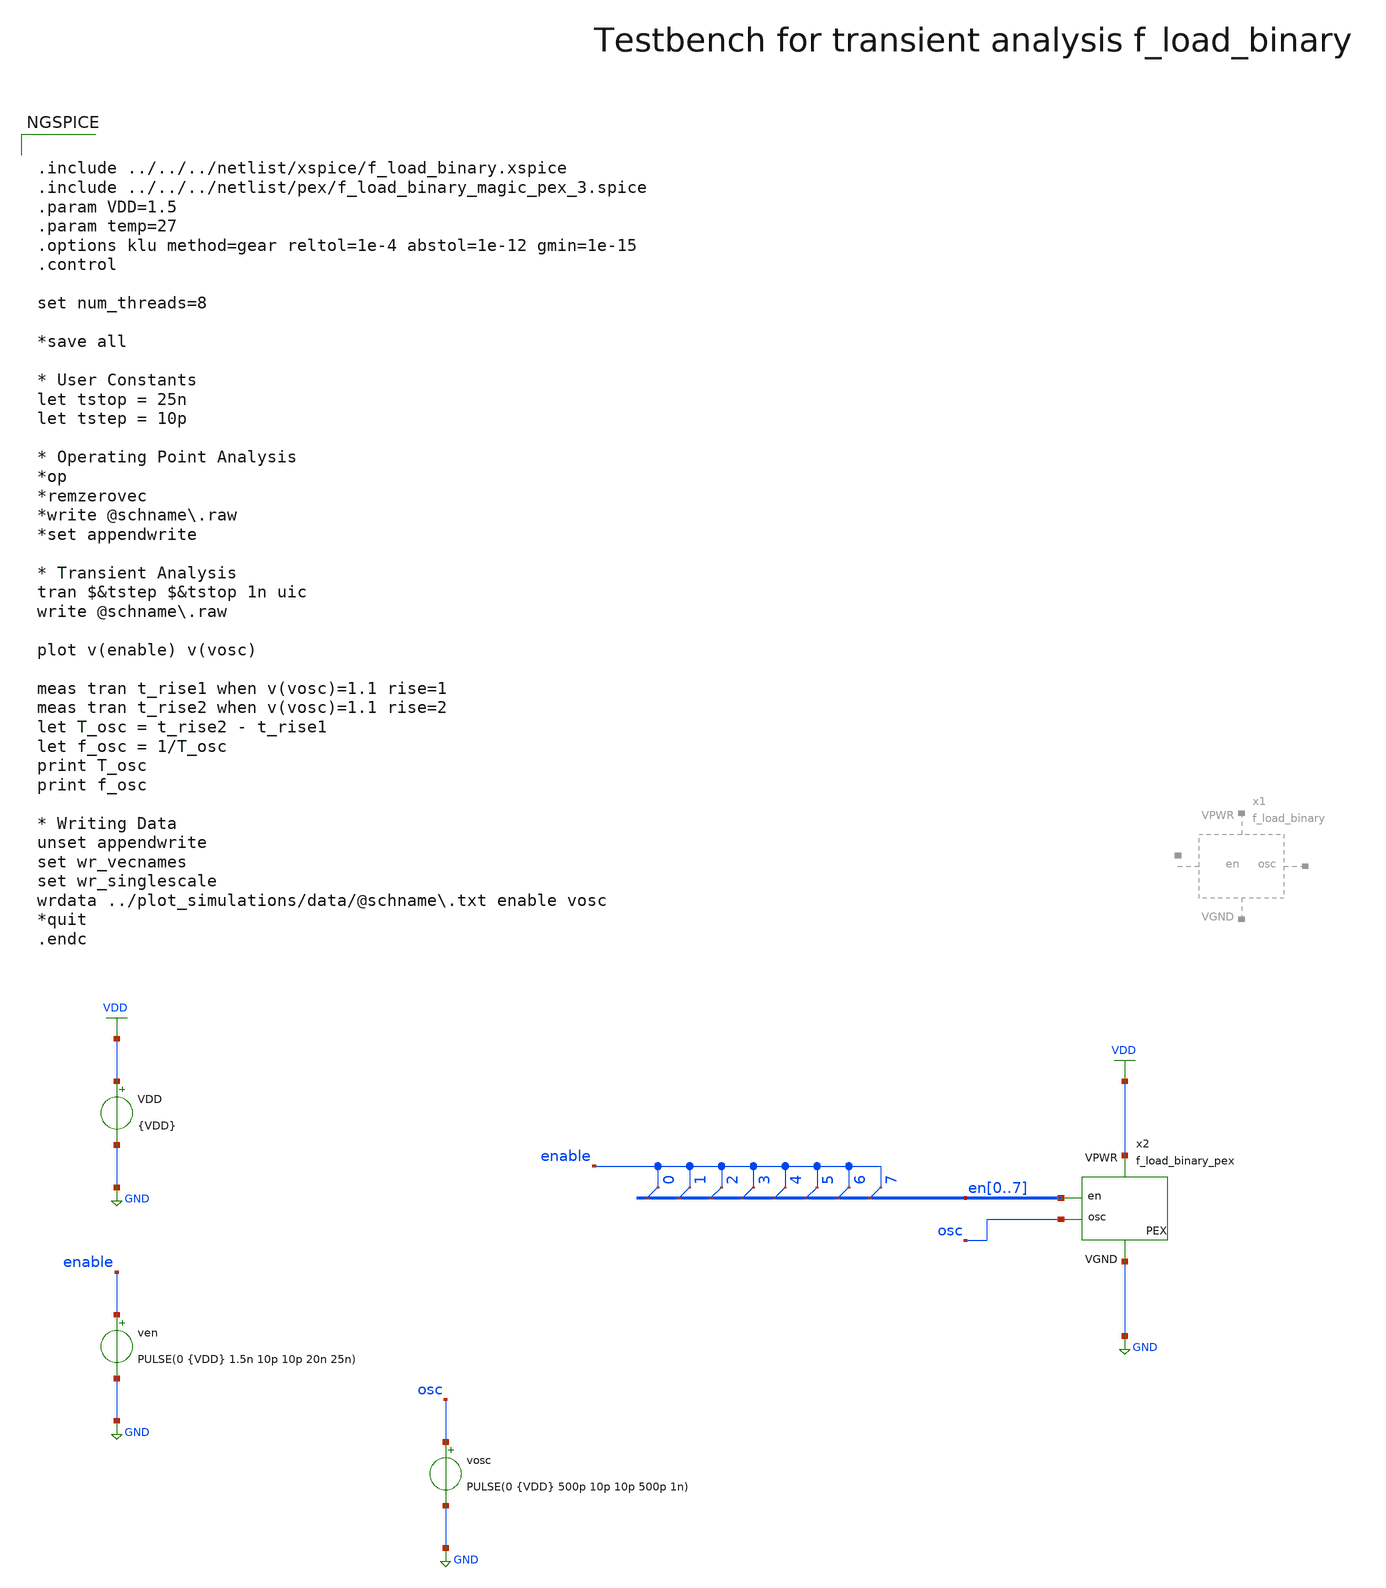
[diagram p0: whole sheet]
** sch_path: macros/heichips26_digital_project/macros/f_load_binary/testbenches/xschem/f_load_binary_tb_tran.sch
**.subckt f_load_binary_tb_tran
VDD VDD GND {VDD}
ven enable GND PULSE(0 {VDD} 1.5n 10p 10p 20n 25n)
x2 VDD GND en0 en1 en2 en3 en4 osc f_load_binary_pex
* tap: en[0..7] --> en1
* tap: en[0..7] --> en1
* tap: en[0..7] --> en1
* tap: en[0..7] --> en1
* tap: en[0..7] --> en1
* tap: en[0..7] --> en1
* tap: en[0..7] --> en1
* tap: en[0..7] --> en1
vosc osc GND PULSE(0 {VDD} 500p 10p 10p 500p 1n)
**** begin user architecture code


.include ../../../netlist/xspice/f_load_binary.xspice
.include ../../../netlist/pex/f_load_binary_magic_pex_3.spice
.param VDD=1.5
.param temp=27
.options klu method=gear reltol=1e-4 abstol=1e-12 gmin=1e-15
.control

set num_threads=8

*save all

* User Constants
let tstop = 25n
let tstep = 10p

* Operating Point Analysis
*op
*remzerovec
*write @schname\.raw
*set appendwrite

* Transient Analysis
tran $&tstep $&tstop 1n uic
write @schname\.raw

plot v(enable) v(vosc)

meas tran t_rise1 when v(vosc)=1.1 rise=1
meas tran t_rise2 when v(vosc)=1.1 rise=2
let T_osc = t_rise2 - t_rise1
let f_osc = 1/T_osc
print T_osc
print f_osc

* Writing Data
unset appendwrite
set wr_vecnames
set wr_singlescale
wrdata ../plot_simulations/data/@schname\.txt enable vosc
*quit
.endc


.lib cornerMOSlv.lib mos_tt
.lib cornerMOShv.lib mos_tt
.lib cornerRES.lib res_typ
.lib cornerDIO.lib dio_tt

**** end user architecture code
**.ends
.GLOBAL GND
.GLOBAL VDD
.end
